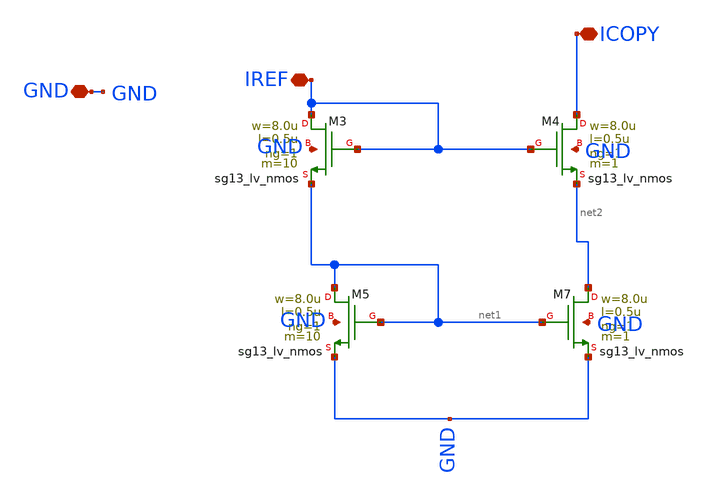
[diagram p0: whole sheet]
** sch_path: blocks/composite/dpi_adexp_neuron/design_data/xschem/sbcmN.sch
**.subckt sbcmN GND IREF ICOPY
*.iopin GND
*.iopin IREF
*.iopin ICOPY
XM3 IREF IREF net1 GND sg13_lv_nmos w=8.0u l=0.5u ng=1 m=10 mm_ok=1
XM4 ICOPY IREF net2 GND sg13_lv_nmos w=8.0u l=0.5u ng=1 m=1 mm_ok=1
XM5 net1 net1 GND GND sg13_lv_nmos w=8.0u l=0.5u ng=1 m=10 mm_ok=1
XM7 net2 net1 GND GND sg13_lv_nmos w=8.0u l=0.5u ng=1 m=1 mm_ok=1
**.ends
.end
